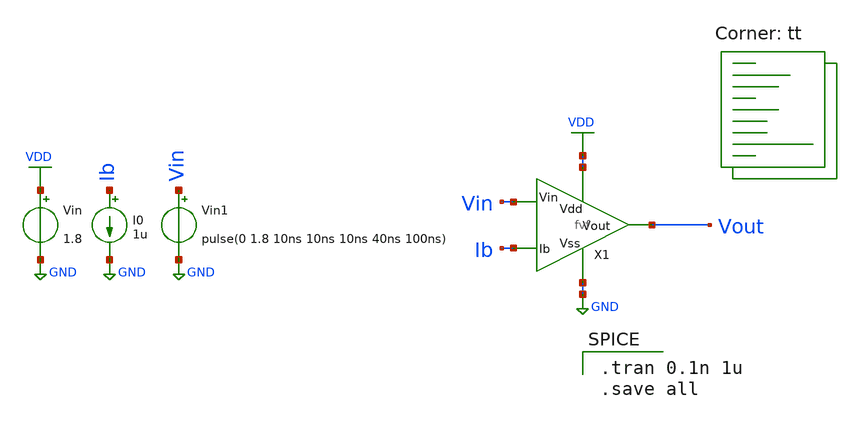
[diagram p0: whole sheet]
** sch_path: xschem/fvf_tb_tran.sch
**.subckt fvf_tb_tran
Vin VDD GND 1.8
I0 Ib GND 1u
X1 VDD GND Vin Vout Ib fvf
Vin1 Vin GND pulse(0 1.8 10ns 10ns 10ns 40ns 100ns)
**** begin user architecture code
.lib $::SKYWATER_MODELS/sky130.lib.spice tt

.tran 0.1n 1u
.save all

**** end user architecture code
**.ends

* expanding   symbol:  /foss/designs/fvf-chipathon-2024/xschem/fvf.sym # of pins=5
** sym_path: xschem/fvf.sym
** sch_path: xschem/fvf.sch
.subckt fvf Vdd Vss Vin Vout Ib
*.ipin Vin
*.ipin Ib
*.opin Vout
*.iopin Vdd
*.iopin Vss
XM1 net1 Vin Vout GND sky130_fd_pr__nfet_01v8 L=1 W=15 nf=1 ad='int((nf+1)/2) * W/nf * 0.29' as='int((nf+2)/2) * W/nf * 0.29'
+ pd='2*int((nf+1)/2) * (W/nf + 0.29)' ps='2*int((nf+2)/2) * (W/nf + 0.29)' nrd='0.29 / W' nrs='0.29 / W'
+ sa=0 sb=0 sd=0 mult=1 m=1
XM2 Vout net1 Vss GND sky130_fd_pr__nfet_01v8 L=1 W=15 nf=1 ad='int((nf+1)/2) * W/nf * 0.29' as='int((nf+2)/2) * W/nf * 0.29'
+ pd='2*int((nf+1)/2) * (W/nf + 0.29)' ps='2*int((nf+2)/2) * (W/nf + 0.29)' nrd='0.29 / W' nrs='0.29 / W'
+ sa=0 sb=0 sd=0 mult=1 m=1
XM3 Ib Ib Vdd VDD sky130_fd_pr__pfet_01v8_lvt L=1 W=2 nf=1 ad='int((nf+1)/2) * W/nf * 0.29' as='int((nf+2)/2) * W/nf * 0.29'
+ pd='2*int((nf+1)/2) * (W/nf + 0.29)' ps='2*int((nf+2)/2) * (W/nf + 0.29)' nrd='0.29 / W' nrs='0.29 / W'
+ sa=0 sb=0 sd=0 mult=1 m=1
XM4 net1 Ib Vdd VDD sky130_fd_pr__pfet_01v8_lvt L=1 W=2 nf=1 ad='int((nf+1)/2) * W/nf * 0.29' as='int((nf+2)/2) * W/nf * 0.29'
+ pd='2*int((nf+1)/2) * (W/nf + 0.29)' ps='2*int((nf+2)/2) * (W/nf + 0.29)' nrd='0.29 / W' nrs='0.29 / W'
+ sa=0 sb=0 sd=0 mult=1 m=1
.ends

.GLOBAL VDD
.GLOBAL GND
.end
